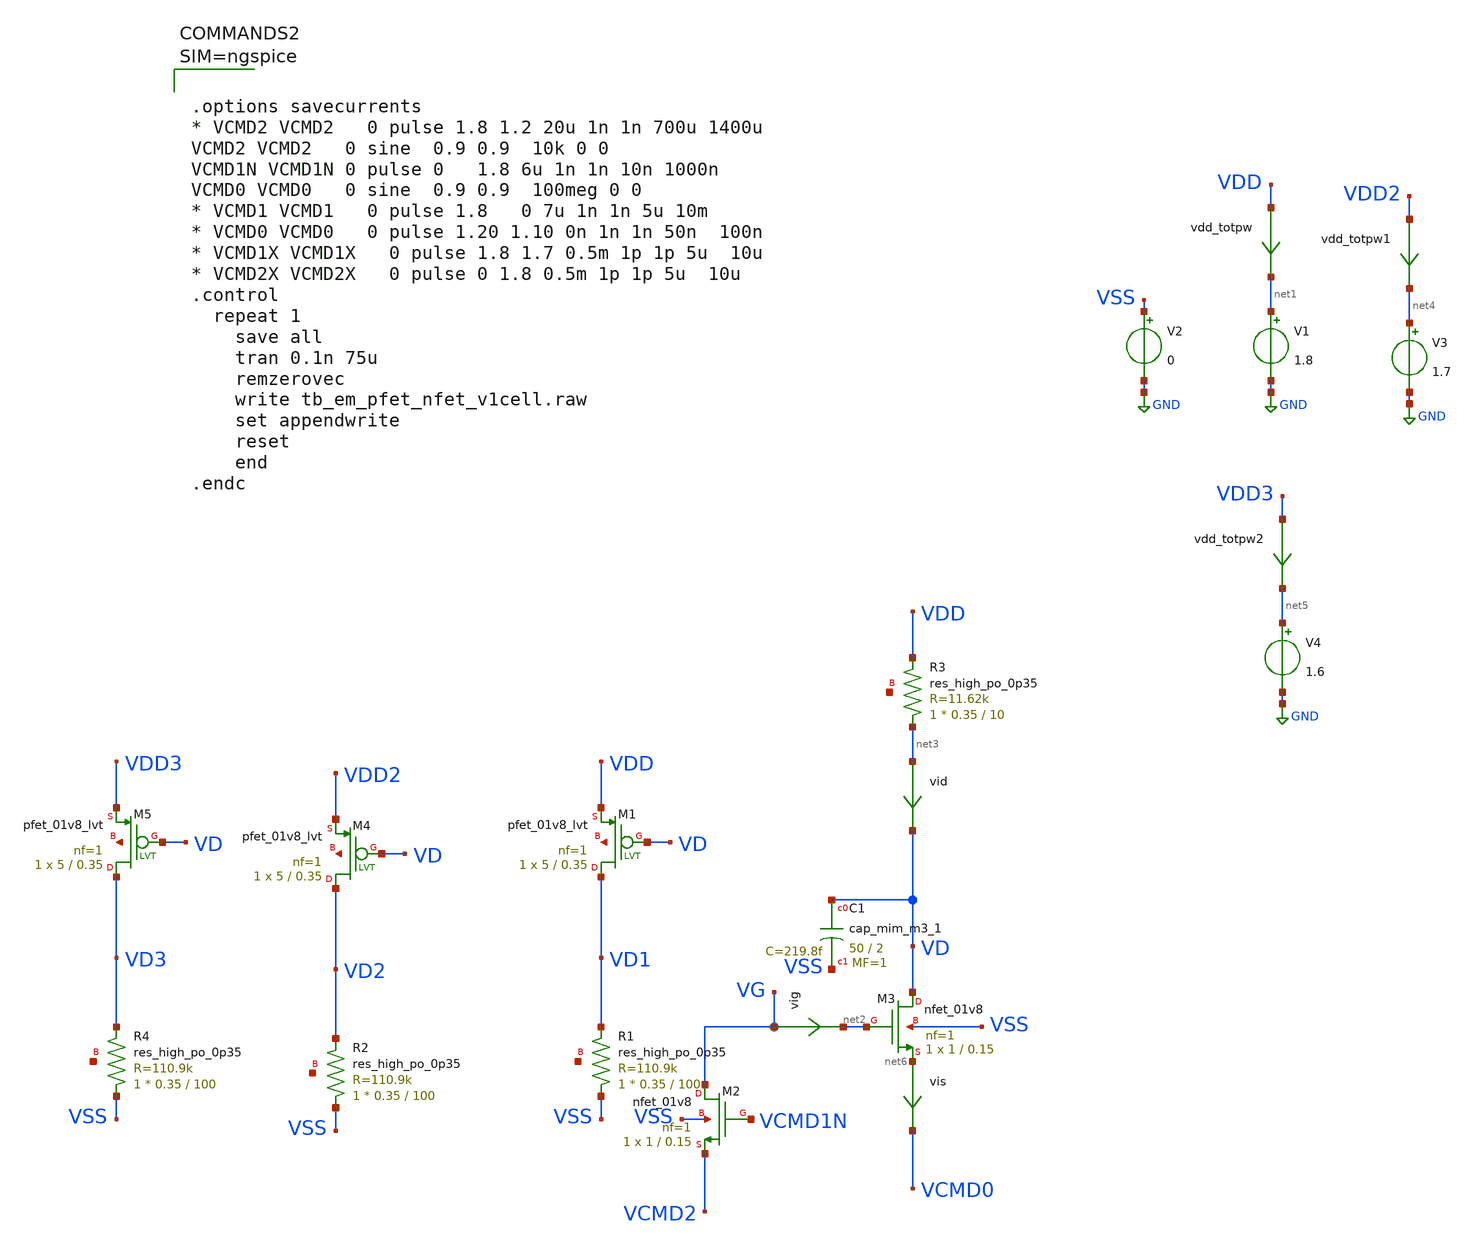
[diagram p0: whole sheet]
** sch_path: xschem/tb_em_pfet_nfet_v1cell.sch
**.subckt tb_em_pfet_nfet_v1cell
V1 net1 GND 1.8
V2 VSS GND 0
vdd_totpw VDD net1 0
.save i(vdd_totpw)
vis net6 VCMD0 0
.save i(vis)
XR3 net3 VDD net7 sky130_fd_pr__res_high_po_0p35 L=10 mult=1 m=1
vig VG net2 0
.save i(vig)
vid net3 VD 0
.save i(vid)
XM3 VD net2 net6 VSS sky130_fd_pr__nfet_01v8 L=0.15 W=1 nf=1 ad='int((nf+1)/2) * W/nf * 0.29' as='int((nf+2)/2) * W/nf * 0.29'
+ pd='2*int((nf+1)/2) * (W/nf + 0.29)' ps='2*int((nf+2)/2) * (W/nf + 0.29)' nrd='0.29 / W' nrs='0.29 / W'
+ sa=0 sb=0 sd=0 mult=1 m=1
XM2 VG VCMD1N VCMD2 VSS sky130_fd_pr__nfet_01v8 L=0.15 W=1 nf=1 ad='int((nf+1)/2) * W/nf * 0.29' as='int((nf+2)/2) * W/nf * 0.29'
+ pd='2*int((nf+1)/2) * (W/nf + 0.29)' ps='2*int((nf+2)/2) * (W/nf + 0.29)' nrd='0.29 / W' nrs='0.29 / W'
+ sa=0 sb=0 sd=0 mult=1 m=1
XC1 VD VSS sky130_fd_pr__cap_mim_m3_1 W=50 L=2 MF=1 m=1
XR1 VSS VD1 net8 sky130_fd_pr__res_high_po_0p35 L=100 mult=1 m=1
XM1 VD1 VD VDD net9 sky130_fd_pr__pfet_01v8_lvt L=0.35 W=5 nf=1 ad='int((nf+1)/2) * W/nf * 0.29' as='int((nf+2)/2) * W/nf * 0.29'
+ pd='2*int((nf+1)/2) * (W/nf + 0.29)' ps='2*int((nf+2)/2) * (W/nf + 0.29)' nrd='0.29 / W' nrs='0.29 / W'
+ sa=0 sb=0 sd=0 mult=1 m=1
XR2 VSS VD2 net10 sky130_fd_pr__res_high_po_0p35 L=100 mult=1 m=1
XM4 VD2 VD VDD2 net11 sky130_fd_pr__pfet_01v8_lvt L=0.35 W=5 nf=1 ad='int((nf+1)/2) * W/nf * 0.29' as='int((nf+2)/2) * W/nf * 0.29'
+ pd='2*int((nf+1)/2) * (W/nf + 0.29)' ps='2*int((nf+2)/2) * (W/nf + 0.29)' nrd='0.29 / W' nrs='0.29 / W'
+ sa=0 sb=0 sd=0 mult=1 m=1
V3 net4 GND 1.7
vdd_totpw1 VDD2 net4 0
.save i(vdd_totpw1)
XR4 VSS VD3 net12 sky130_fd_pr__res_high_po_0p35 L=100 mult=1 m=1
XM5 VD3 VD VDD3 net13 sky130_fd_pr__pfet_01v8_lvt L=0.35 W=5 nf=1 ad='int((nf+1)/2) * W/nf * 0.29' as='int((nf+2)/2) * W/nf * 0.29'
+ pd='2*int((nf+1)/2) * (W/nf + 0.29)' ps='2*int((nf+2)/2) * (W/nf + 0.29)' nrd='0.29 / W' nrs='0.29 / W'
+ sa=0 sb=0 sd=0 mult=1 m=1
V4 net5 GND 1.6
vdd_totpw2 VDD3 net5 0
.save i(vdd_totpw2)
**** begin user architecture code

** opencircuitdesign pdks install
.lib $::SKYWATER_MODELS/sky130.lib.spice tt_mm
*.lib $::SKYWATER_STDCELLS/sky130_fd_sc_hd_blablabla.spice

.subckt sky130_fd_sc_hd__inv_1 A VGND VNB VPB VPWR Y
X0 VGND A Y VNB sky130_fd_pr__nfet_01v8 w=650000u l=150000u
X1 VPWR A Y VPB sky130_fd_pr__pfet_01v8_hvt w=1e+06u l=150000u
.ends





.options savecurrents
* VCMD2 VCMD2   0 pulse 1.8 1.2 20u 1n 1n 700u 1400u
VCMD2 VCMD2   0 sine  0.9 0.9  10k 0 0
VCMD1N VCMD1N 0 pulse 0   1.8 6u 1n 1n 10n 1000n
VCMD0 VCMD0   0 sine  0.9 0.9  100meg 0 0
* VCMD1 VCMD1   0 pulse 1.8   0 7u 1n 1n 5u 10m
* VCMD0 VCMD0   0 pulse 1.20 1.10 0n 1n 1n 50n  100n
* VCMD1X VCMD1X   0 pulse 1.8 1.7 0.5m 1p 1p 5u  10u
* VCMD2X VCMD2X   0 pulse 0 1.8 0.5m 1p 1p 5u  10u
.control
  repeat 1
    save all
    tran 0.1n 75u
    remzerovec
    write tb_em_pfet_nfet_v1cell.raw
    set appendwrite
    reset
    end
.endc



**** end user architecture code
**.ends
.GLOBAL GND
.end
